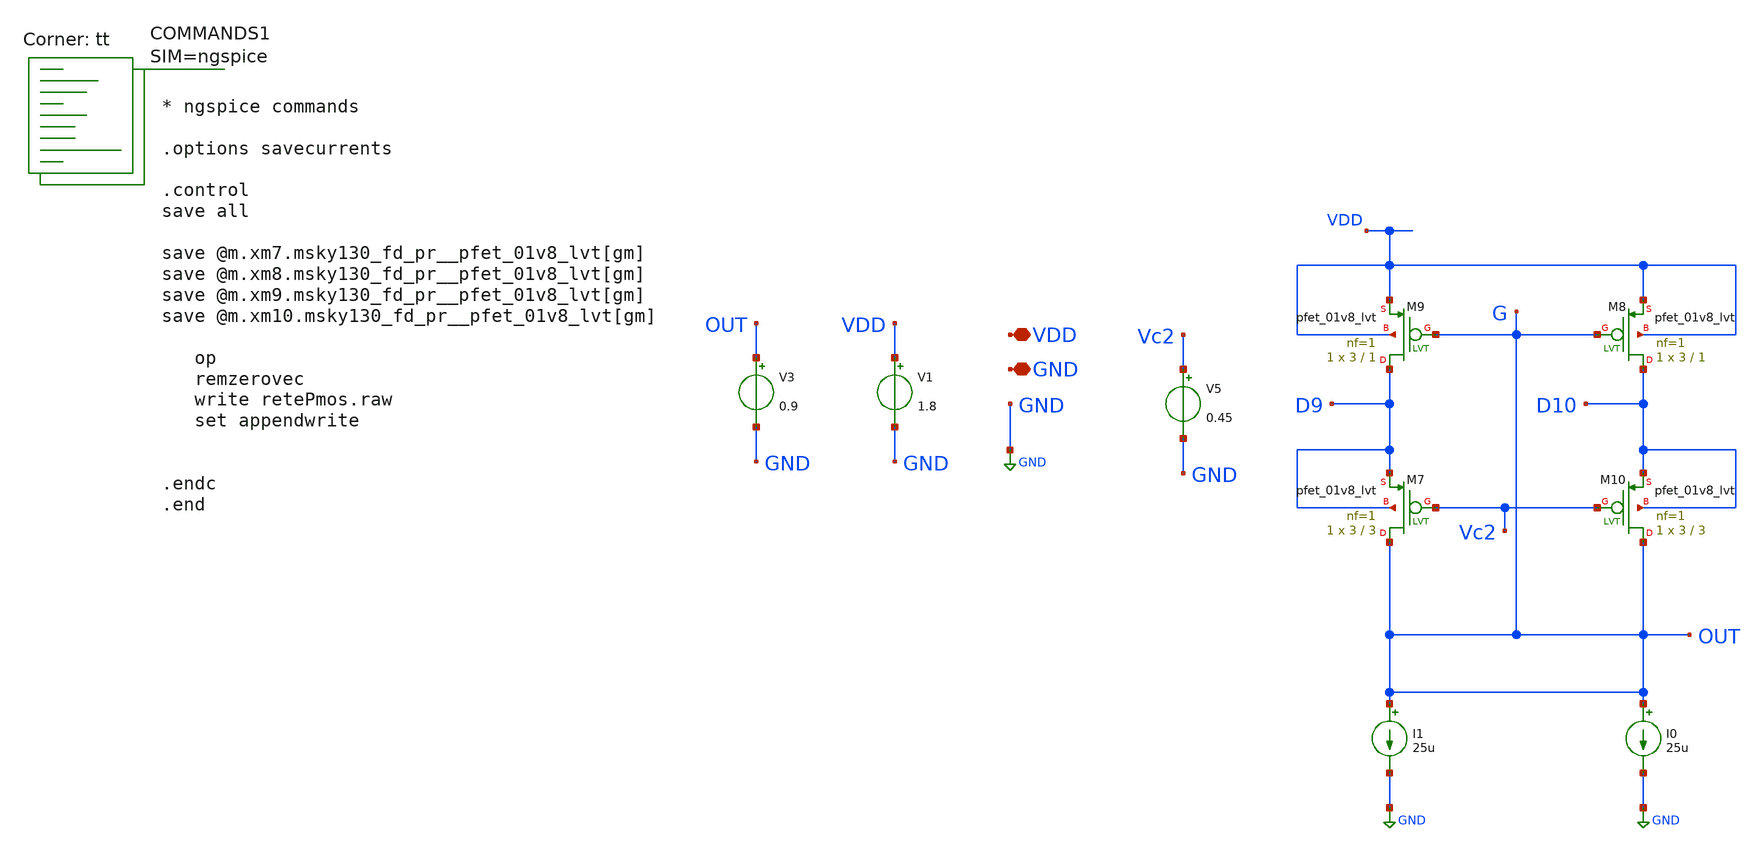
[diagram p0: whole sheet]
** sch_path: xschem/retePmos.sch
**.subckt retePmos VDD GND
*.iopin VDD
*.iopin GND
XM7 G Vc2 D9 D9 sky130_fd_pr__pfet_01v8_lvt L=3 W=3 nf=1 ad='int((nf+1)/2) * W/nf * 0.29' as='int((nf+2)/2) * W/nf * 0.29'
+ pd='2*int((nf+1)/2) * (W/nf + 0.29)' ps='2*int((nf+2)/2) * (W/nf + 0.29)' nrd='0.29 / W' nrs='0.29 / W'
+ sa=0 sb=0 sd=0 mult=1 m=1
XM9 D9 G VDD VDD sky130_fd_pr__pfet_01v8_lvt L=1 W=3 nf=1 ad='int((nf+1)/2) * W/nf * 0.29' as='int((nf+2)/2) * W/nf * 0.29'
+ pd='2*int((nf+1)/2) * (W/nf + 0.29)' ps='2*int((nf+2)/2) * (W/nf + 0.29)' nrd='0.29 / W' nrs='0.29 / W'
+ sa=0 sb=0 sd=0 mult=1 m=1
XM8 D10 G VDD VDD sky130_fd_pr__pfet_01v8_lvt L=1 W=3 nf=1 ad='int((nf+1)/2) * W/nf * 0.29' as='int((nf+2)/2) * W/nf * 0.29'
+ pd='2*int((nf+1)/2) * (W/nf + 0.29)' ps='2*int((nf+2)/2) * (W/nf + 0.29)' nrd='0.29 / W' nrs='0.29 / W'
+ sa=0 sb=0 sd=0 mult=1 m=1
XM10 G Vc2 D10 D10 sky130_fd_pr__pfet_01v8_lvt L=3 W=3 nf=1 ad='int((nf+1)/2) * W/nf * 0.29' as='int((nf+2)/2) * W/nf * 0.29'
+ pd='2*int((nf+1)/2) * (W/nf + 0.29)' ps='2*int((nf+2)/2) * (W/nf + 0.29)' nrd='0.29 / W' nrs='0.29 / W'
+ sa=0 sb=0 sd=0 mult=1 m=1
V1 VDD GND 1.8
V3 OUT GND 0.9
V5 Vc2 GND 0.45
I0 G GND 25u
I1 G GND 25u
**** begin user architecture code



* ngspice commands

.options savecurrents

.control
save all

save @m.xm7.msky130_fd_pr__pfet_01v8_lvt[gm]
save @m.xm8.msky130_fd_pr__pfet_01v8_lvt[gm]
save @m.xm9.msky130_fd_pr__pfet_01v8_lvt[gm]
save @m.xm10.msky130_fd_pr__pfet_01v8_lvt[gm]

   op
   remzerovec
   write retePmos.raw
   set appendwrite


.endc
.end



.lib $::SKYWATER_MODELS/sky130.lib.spice tt
**** end user architecture code
**.ends
.GLOBAL GND
.end
